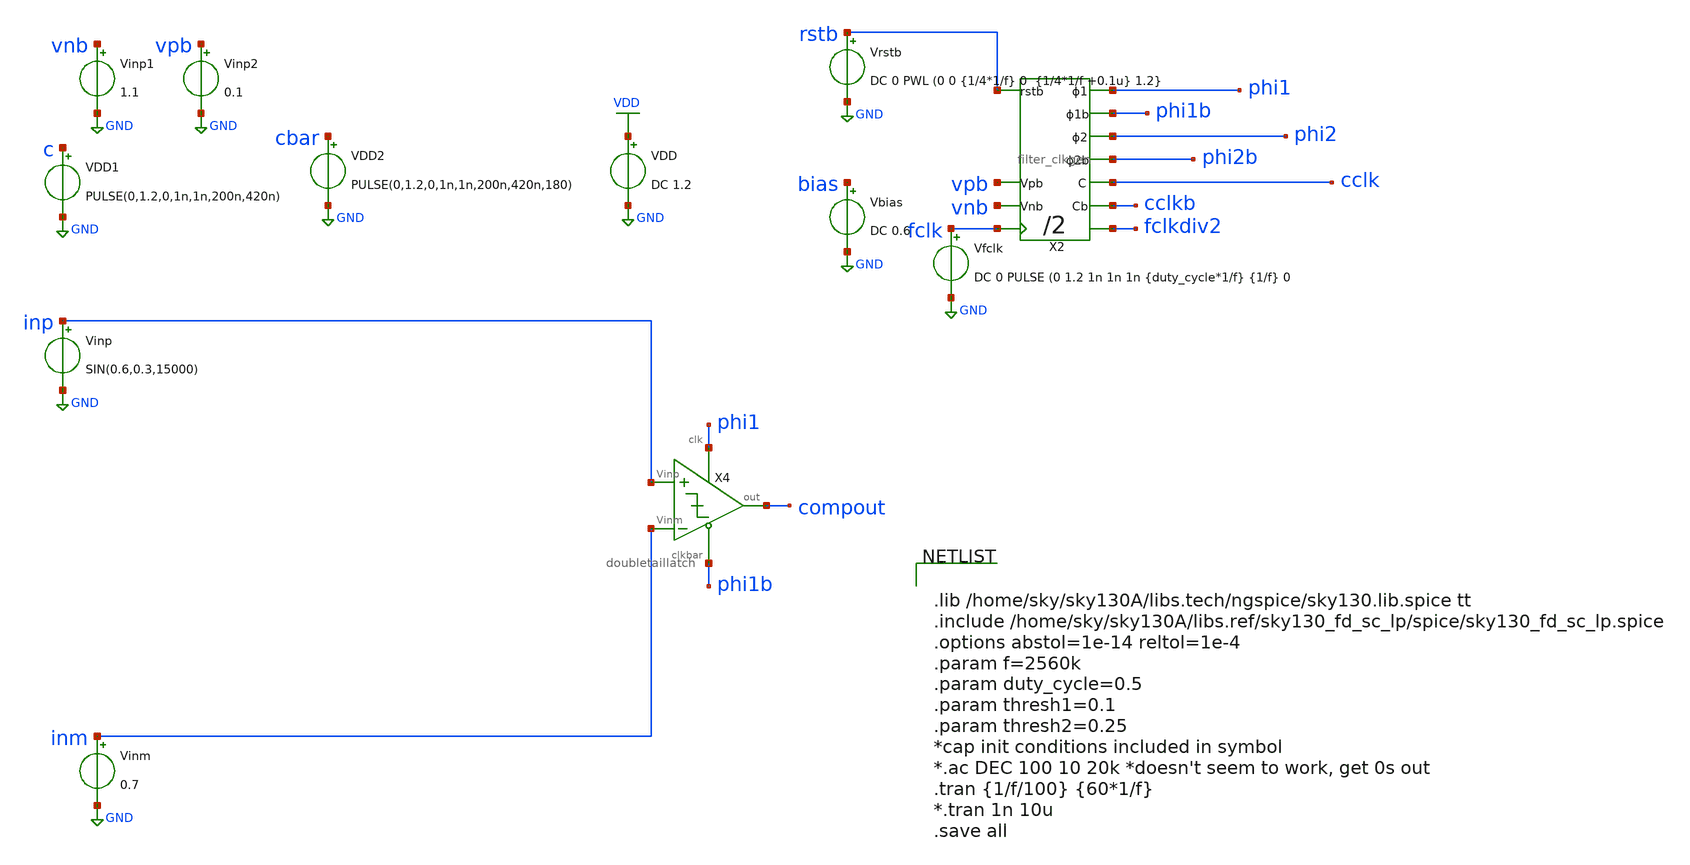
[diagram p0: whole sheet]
** sch_path: xschem/comparator/NotWorking.sch
**.subckt NotWorking
Vinp inp GND SIN(0.6,0.3,15000)
VDD VDD GND DC 1.2
Vinm inm GND 0.7
X4 inp inm compout phi1 phi1b doubletaillatch
VDD1 c GND PULSE(0,1.2,0,1n,1n,200n,420n)
VDD2 cbar GND PULSE(0,1.2,0,1n,1n,200n,420n,180)
Vfclk fclk GND DC 0 PULSE (0 1.2 1n 1n 1n {duty_cycle*1/f} {1/f} 0
X2 rstb fclk phi2b phi2 phi1b phi1 cclkb cclk fclkdiv2 vpb vnb filter_clkgen
Vbias bias GND DC 0.6
Vrstb rstb GND DC 0 PWL (0 0 {1/4*1/f} 0 {1/4*1/f +0.1u} 1.2}
Vinp1 vnb GND 1.1
Vinp2 vpb GND 0.1
**** begin user architecture code


.lib /home/sky/sky130A/libs.tech/ngspice/sky130.lib.spice tt
.include /home/sky/sky130A/libs.ref/sky130_fd_sc_lp/spice/sky130_fd_sc_lp.spice
.options abstol=1e-14 reltol=1e-4
.param f=2560k
.param duty_cycle=0.5
.param thresh1=0.1
.param thresh2=0.25
*cap init conditions included in symbol
*.ac DEC 100 10 20k *doesn't seem to work, get 0s out
.tran {1/f/100} {60*1/f}
*.tran 1n 10u
.save all


**** end user architecture code
**.ends
.GLOBAL GND
.GLOBAL VDD
.end
